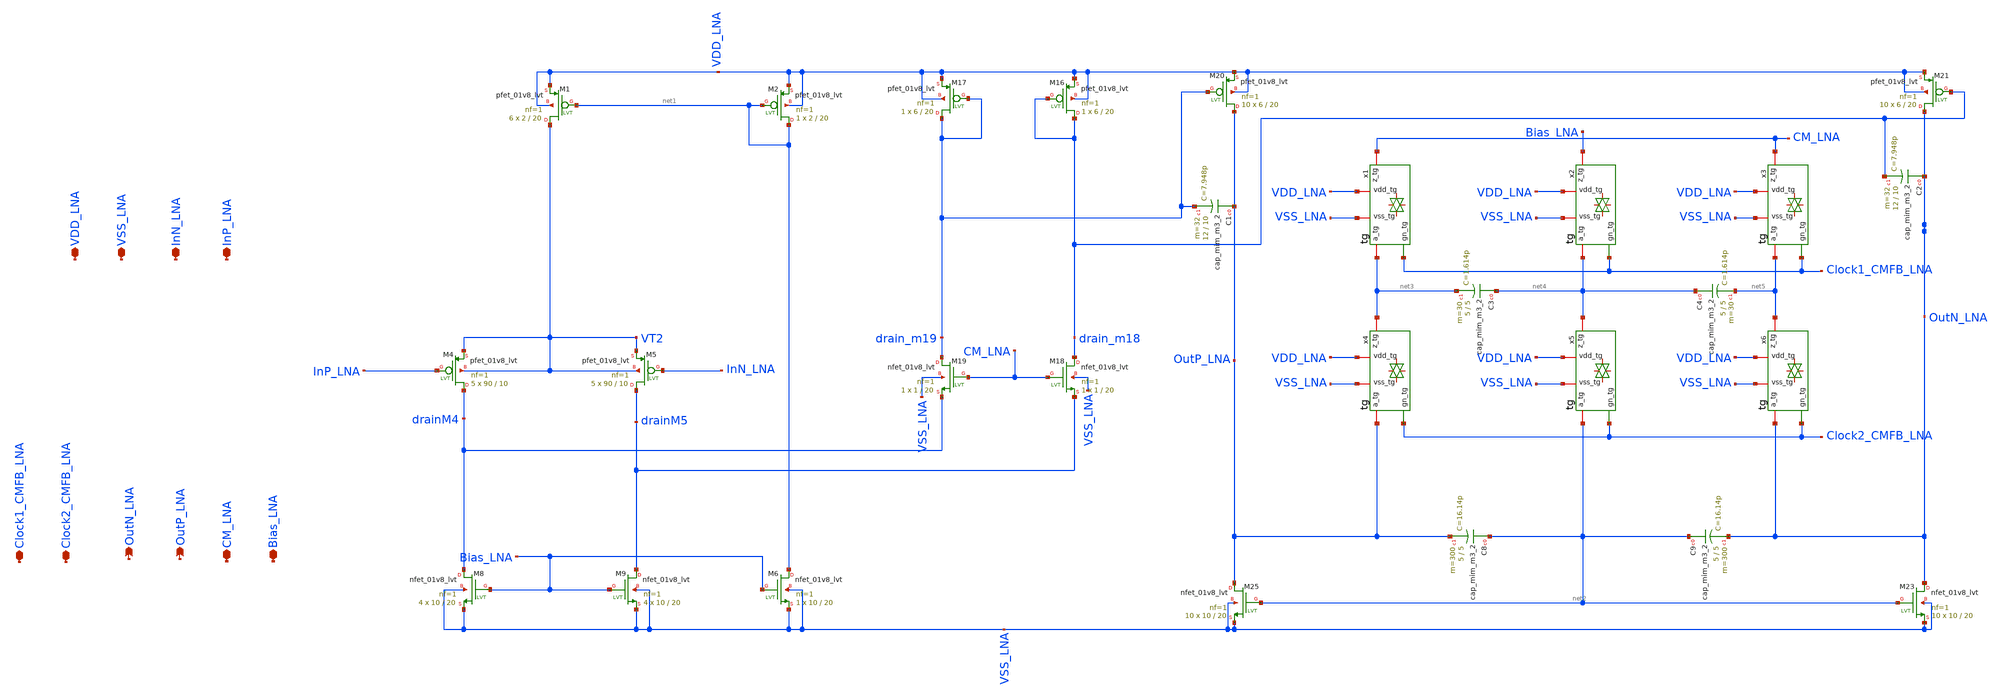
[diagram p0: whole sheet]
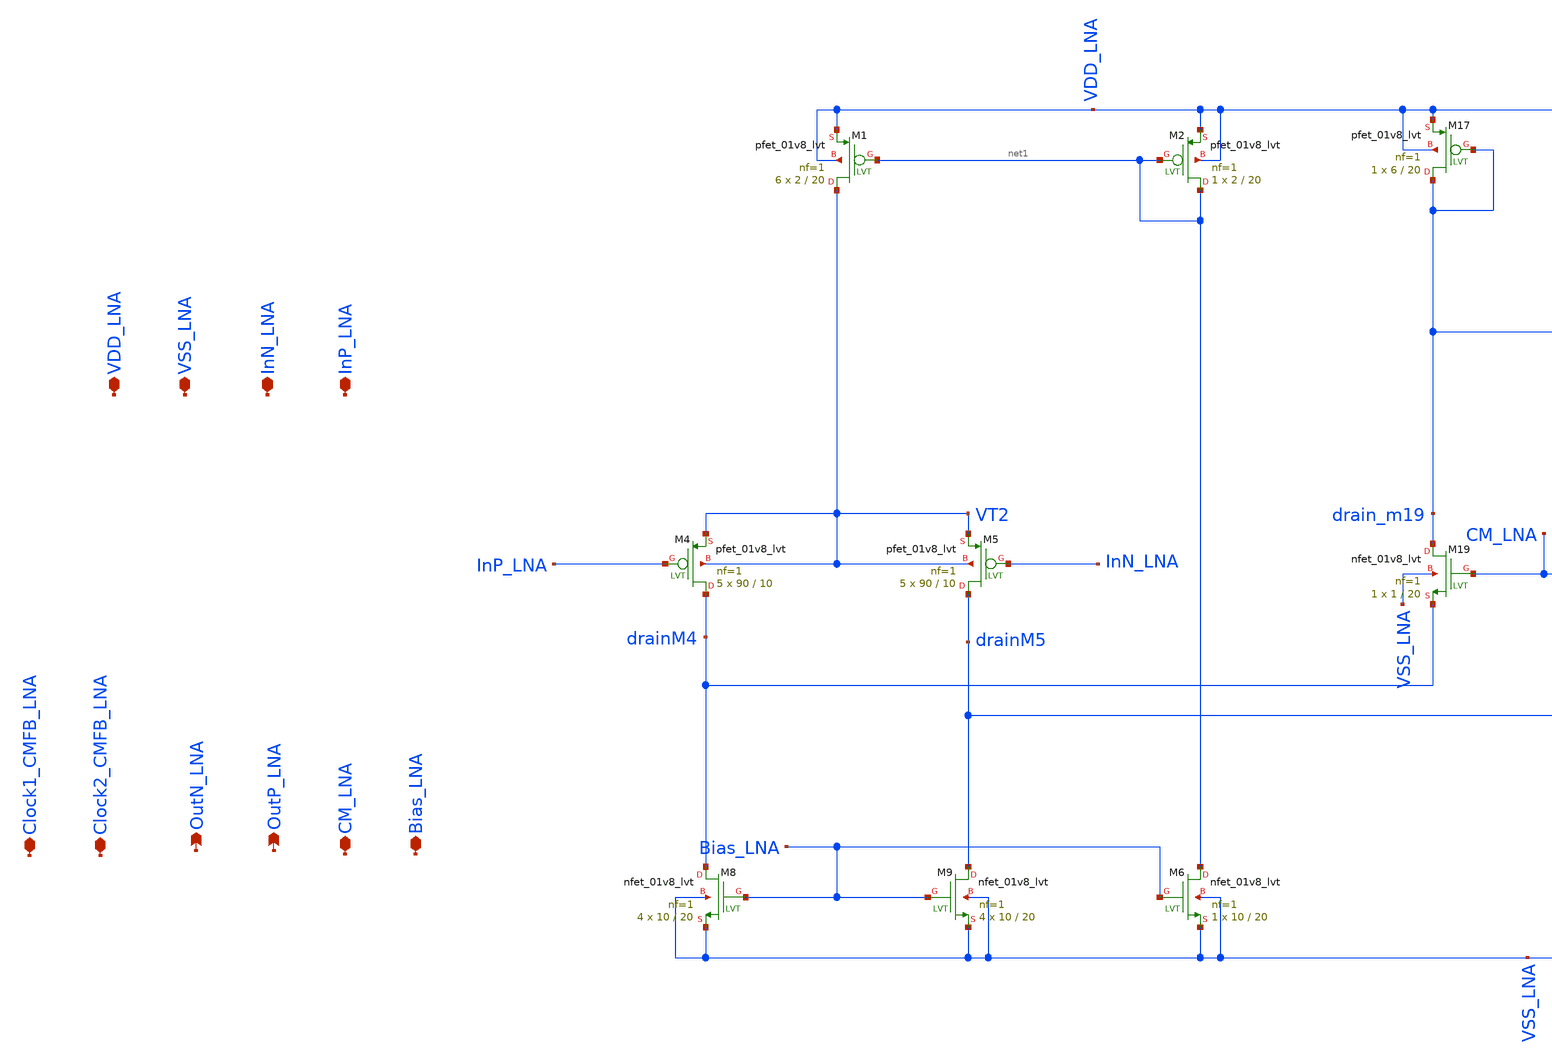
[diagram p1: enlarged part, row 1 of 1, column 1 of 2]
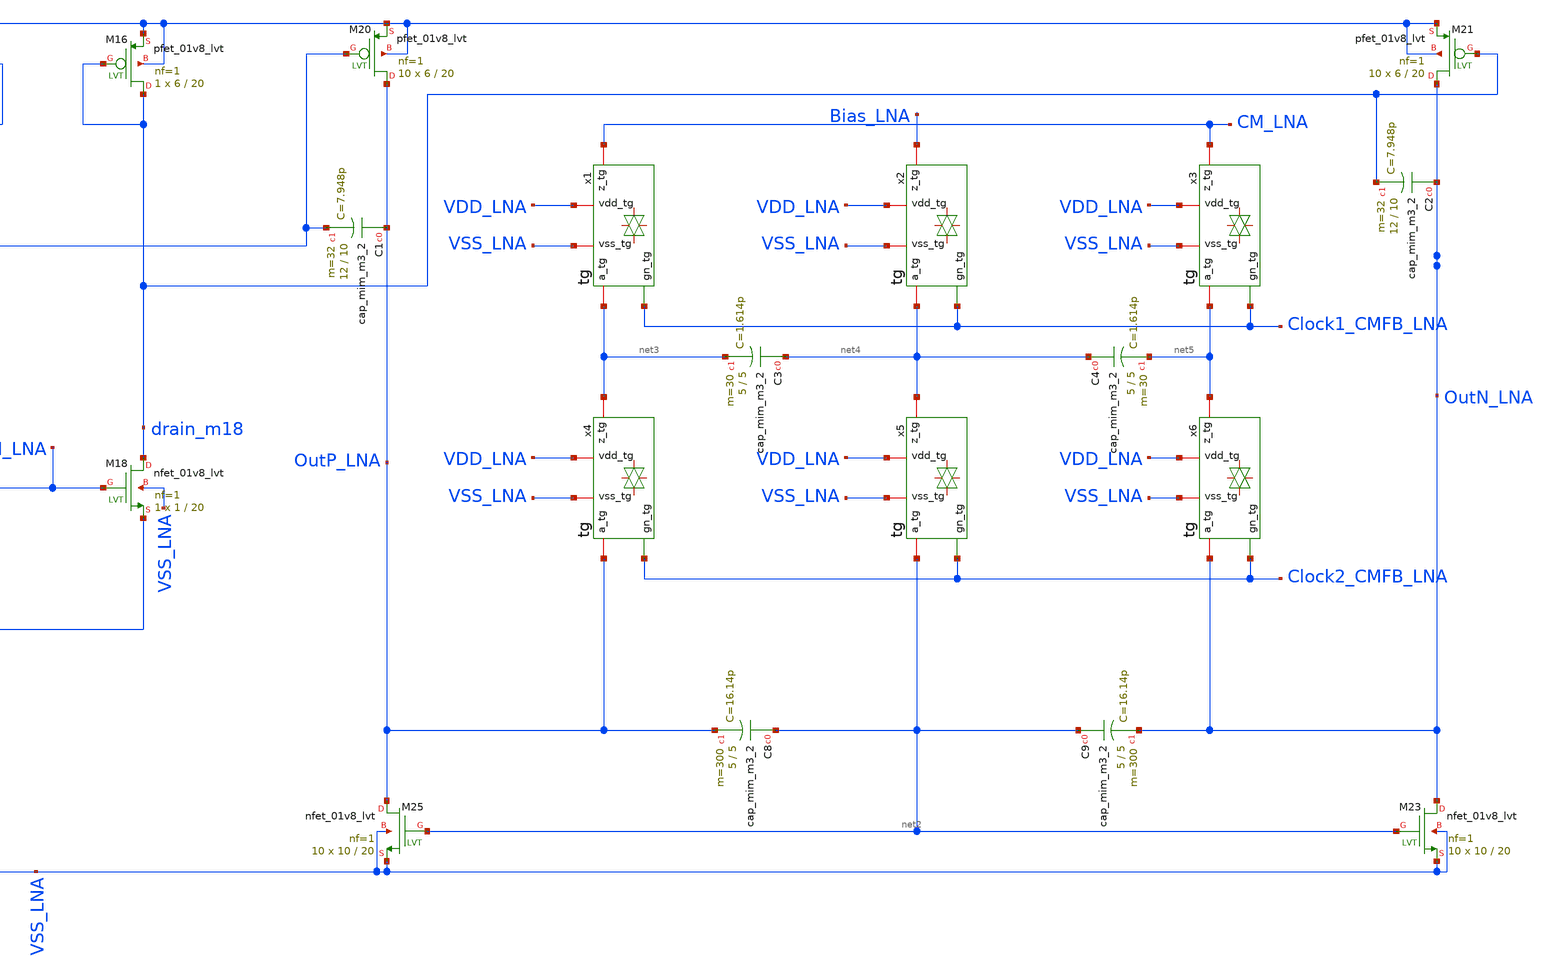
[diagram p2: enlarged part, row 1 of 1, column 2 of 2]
** sch_path: LNA.sch
**.subckt LNA InP_LNA InN_LNA VSS_LNA VDD_LNA CM_LNA OutP_LNA OutN_LNA Clock2_CMFB_LNA Bias_LNA
*+ Clock1_CMFB_LNA
*.iopin InP_LNA
*.iopin InN_LNA
*.iopin VSS_LNA
*.iopin VDD_LNA
*.iopin CM_LNA
*.opin OutP_LNA
*.opin OutN_LNA
*.iopin Clock2_CMFB_LNA
*.iopin Bias_LNA
*.iopin Clock1_CMFB_LNA
XM4 drainM4 InP_LNA VT2 VT2 sky130_fd_pr__pfet_01v8_lvt L=10 W=90 nf=1 ad='int((nf+1)/2) * W/nf * 0.29'
+ as='int((nf+2)/2) * W/nf * 0.29' pd='2*int((nf+1)/2) * (W/nf + 0.29)' ps='2*int((nf+2)/2) * (W/nf + 0.29)'
+ nrd='0.29 / W' nrs='0.29 / W' sa=0 sb=0 sd=0 mult=5 m=5
XM5 drainM5 InN_LNA VT2 VT2 sky130_fd_pr__pfet_01v8_lvt L=10 W=90 nf=1 ad='int((nf+1)/2) * W/nf * 0.29'
+ as='int((nf+2)/2) * W/nf * 0.29' pd='2*int((nf+1)/2) * (W/nf + 0.29)' ps='2*int((nf+2)/2) * (W/nf + 0.29)'
+ nrd='0.29 / W' nrs='0.29 / W' sa=0 sb=0 sd=0 mult=5 m=5
XM8 drainM4 Bias_LNA VSS_LNA VSS_LNA sky130_fd_pr__nfet_01v8_lvt L=20 W=10 nf=1 ad='int((nf+1)/2) * W/nf * 0.29'
+ as='int((nf+2)/2) * W/nf * 0.29' pd='2*int((nf+1)/2) * (W/nf + 0.29)' ps='2*int((nf+2)/2) * (W/nf + 0.29)'
+ nrd='0.29 / W' nrs='0.29 / W' sa=0 sb=0 sd=0 mult=4 m=4
XM9 drainM5 Bias_LNA VSS_LNA VSS_LNA sky130_fd_pr__nfet_01v8_lvt L=20 W=10 nf=1 ad='int((nf+1)/2) * W/nf * 0.29'
+ as='int((nf+2)/2) * W/nf * 0.29' pd='2*int((nf+1)/2) * (W/nf + 0.29)' ps='2*int((nf+2)/2) * (W/nf + 0.29)'
+ nrd='0.29 / W' nrs='0.29 / W' sa=0 sb=0 sd=0 mult=4 m=4
XM16 drain_m18 drain_m18 VDD_LNA VDD_LNA sky130_fd_pr__pfet_01v8_lvt L=20 W=6 nf=1 ad='int((nf+1)/2) * W/nf * 0.29'
+ as='int((nf+2)/2) * W/nf * 0.29' pd='2*int((nf+1)/2) * (W/nf + 0.29)' ps='2*int((nf+2)/2) * (W/nf + 0.29)'
+ nrd='0.29 / W' nrs='0.29 / W' sa=0 sb=0 sd=0 mult=1 m=1
XM17 drain_m19 drain_m19 VDD_LNA VDD_LNA sky130_fd_pr__pfet_01v8_lvt L=20 W=6 nf=1 ad='int((nf+1)/2) * W/nf * 0.29'
+ as='int((nf+2)/2) * W/nf * 0.29' pd='2*int((nf+1)/2) * (W/nf + 0.29)' ps='2*int((nf+2)/2) * (W/nf + 0.29)'
+ nrd='0.29 / W' nrs='0.29 / W' sa=0 sb=0 sd=0 mult=1 m=1
XM18 drain_m18 CM_LNA drainM5 VSS_LNA sky130_fd_pr__nfet_01v8_lvt L=20 W=1 nf=1 ad='int((nf+1)/2) * W/nf * 0.29'
+ as='int((nf+2)/2) * W/nf * 0.29' pd='2*int((nf+1)/2) * (W/nf + 0.29)' ps='2*int((nf+2)/2) * (W/nf + 0.29)'
+ nrd='0.29 / W' nrs='0.29 / W' sa=0 sb=0 sd=0 mult=1 m=1
XM19 drain_m19 CM_LNA drainM4 VSS_LNA sky130_fd_pr__nfet_01v8_lvt L=20 W=1 nf=1 ad='int((nf+1)/2) * W/nf * 0.29'
+ as='int((nf+2)/2) * W/nf * 0.29' pd='2*int((nf+1)/2) * (W/nf + 0.29)' ps='2*int((nf+2)/2) * (W/nf + 0.29)'
+ nrd='0.29 / W' nrs='0.29 / W' sa=0 sb=0 sd=0 mult=1 m=1
XM20 OutP_LNA drain_m19 VDD_LNA VDD_LNA sky130_fd_pr__pfet_01v8_lvt L=20 W=6 nf=1 ad='int((nf+1)/2) * W/nf * 0.29'
+ as='int((nf+2)/2) * W/nf * 0.29' pd='2*int((nf+1)/2) * (W/nf + 0.29)' ps='2*int((nf+2)/2) * (W/nf + 0.29)'
+ nrd='0.29 / W' nrs='0.29 / W' sa=0 sb=0 sd=0 mult=10 m=10
XM21 OutN_LNA drain_m18 VDD_LNA VDD_LNA sky130_fd_pr__pfet_01v8_lvt L=20 W=6 nf=1 ad='int((nf+1)/2) * W/nf * 0.29'
+ as='int((nf+2)/2) * W/nf * 0.29' pd='2*int((nf+1)/2) * (W/nf + 0.29)' ps='2*int((nf+2)/2) * (W/nf + 0.29)'
+ nrd='0.29 / W' nrs='0.29 / W' sa=0 sb=0 sd=0 mult=10 m=10
XM23 OutN_LNA net2 VSS_LNA VSS_LNA sky130_fd_pr__nfet_01v8_lvt L=20 W=10 nf=1 ad='int((nf+1)/2) * W/nf * 0.29'
+ as='int((nf+2)/2) * W/nf * 0.29' pd='2*int((nf+1)/2) * (W/nf + 0.29)' ps='2*int((nf+2)/2) * (W/nf + 0.29)'
+ nrd='0.29 / W' nrs='0.29 / W' sa=0 sb=0 sd=0 mult=10 m=10
XM25 OutP_LNA net2 VSS_LNA VSS_LNA sky130_fd_pr__nfet_01v8_lvt L=20 W=10 nf=1 ad='int((nf+1)/2) * W/nf * 0.29'
+ as='int((nf+2)/2) * W/nf * 0.29' pd='2*int((nf+1)/2) * (W/nf + 0.29)' ps='2*int((nf+2)/2) * (W/nf + 0.29)'
+ nrd='0.29 / W' nrs='0.29 / W' sa=0 sb=0 sd=0 mult=10 m=10
XM1 VT2 net1 VDD_LNA VDD_LNA sky130_fd_pr__pfet_01v8_lvt L=20 W=2 nf=1 ad='int((nf+1)/2) * W/nf * 0.29'
+ as='int((nf+2)/2) * W/nf * 0.29' pd='2*int((nf+1)/2) * (W/nf + 0.29)' ps='2*int((nf+2)/2) * (W/nf + 0.29)'
+ nrd='0.29 / W' nrs='0.29 / W' sa=0 sb=0 sd=0 mult=6 m=6
XM2 net1 net1 VDD_LNA VDD_LNA sky130_fd_pr__pfet_01v8_lvt L=20 W=2 nf=1 ad='int((nf+1)/2) * W/nf * 0.29'
+ as='int((nf+2)/2) * W/nf * 0.29' pd='2*int((nf+1)/2) * (W/nf + 0.29)' ps='2*int((nf+2)/2) * (W/nf + 0.29)'
+ nrd='0.29 / W' nrs='0.29 / W' sa=0 sb=0 sd=0 mult=1 m=1
XM6 net1 Bias_LNA VSS_LNA VSS_LNA sky130_fd_pr__nfet_01v8_lvt L=20 W=10 nf=1 ad='int((nf+1)/2) * W/nf * 0.29'
+ as='int((nf+2)/2) * W/nf * 0.29' pd='2*int((nf+1)/2) * (W/nf + 0.29)' ps='2*int((nf+2)/2) * (W/nf + 0.29)'
+ nrd='0.29 / W' nrs='0.29 / W' sa=0 sb=0 sd=0 mult=1 m=1
XC3 net4 net3 sky130_fd_pr__cap_mim_m3_2 W=5 L=5 MF=30 m=30
XC4 net4 net5 sky130_fd_pr__cap_mim_m3_2 W=5 L=5 MF=30 m=30
XC8 net2 OutP_LNA sky130_fd_pr__cap_mim_m3_2 W=5 L=5 MF=300 m=300
XC9 net2 OutN_LNA sky130_fd_pr__cap_mim_m3_2 W=5 L=5 MF=300 m=300
x1 VDD_LNA net3 CM_LNA VSS_LNA Clock1_CMFB_LNA tg
x2 VDD_LNA net4 Bias_LNA VSS_LNA Clock1_CMFB_LNA tg
x3 VDD_LNA net5 CM_LNA VSS_LNA Clock1_CMFB_LNA tg
x4 VDD_LNA OutP_LNA net3 VSS_LNA Clock2_CMFB_LNA tg
x5 VDD_LNA net2 net4 VSS_LNA Clock2_CMFB_LNA tg
x6 VDD_LNA OutN_LNA net5 VSS_LNA Clock2_CMFB_LNA tg
XC1 OutP_LNA drain_m19 sky130_fd_pr__cap_mim_m3_2 W=12 L=10 MF=32 m=32
XC2 OutN_LNA drain_m18 sky130_fd_pr__cap_mim_m3_2 W=12 L=10 MF=32 m=32
**.ends

* expanding   symbol:  LNA/tg.sym # of pins=5
** sym_path: tg.sym
** sch_path: tg.sch
.subckt tg vdd_tg a_tg z_tg vss_tg gn_tg
*.iopin a_tg
*.iopin z_tg
*.ipin gn_tg
*.iopin vss_tg
*.iopin vdd_tg
XM1 a_tg gn_tg z_tg vss_tg sky130_fd_pr__nfet_01v8 L=0.2 W=1 nf=1 ad='int((nf+1)/2) * W/nf * 0.29' as='int((nf+2)/2) * W/nf * 0.29'
+ pd='2*int((nf+1)/2) * (W/nf + 0.29)' ps='2*int((nf+2)/2) * (W/nf + 0.29)' nrd='0.29 / W' nrs='0.29 / W'
+ sa=0 sb=0 sd=0 mult=1 m=1
XM2 a_tg net1 z_tg vdd_tg sky130_fd_pr__pfet_01v8 L=0.2 W=2 nf=2 ad='int((nf+1)/2) * W/nf * 0.29' as='int((nf+2)/2) * W/nf * 0.29'
+ pd='2*int((nf+1)/2) * (W/nf + 0.29)' ps='2*int((nf+2)/2) * (W/nf + 0.29)' nrd='0.29 / W' nrs='0.29 / W'
+ sa=0 sb=0 sd=0 mult=1 m=1
x10 gn_tg vss_tg vss_tg vdd_tg vdd_tg net1 sky130_fd_sc_hd__inv_1
.ends

.end
